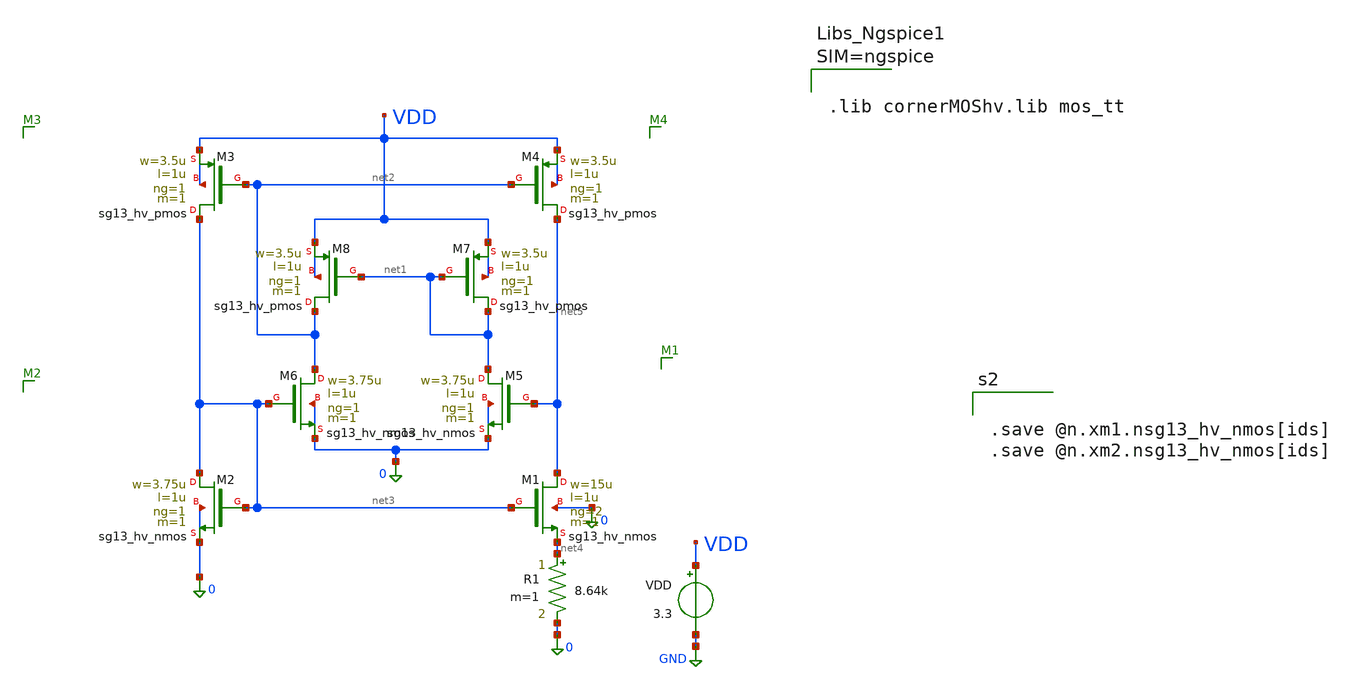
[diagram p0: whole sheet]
** sch_path: v2_bmr_bias/BMR12u5.sch
**.subckt BMR12u5
VDD VDD GND 3.3
R1 net4 0 8.64k m=1
XM1 net5 net3 net4 0 sg13_hv_nmos w=15u l=1u ng=2 m=1 mm_ok=1
XM2 net3 net3 0 0 sg13_hv_nmos w=3.75u l=1u ng=1 m=1 mm_ok=1
XM3 net3 net2 VDD VDD sg13_hv_pmos w=3.5u l=1u ng=1 m=1 mm_ok=1
XM4 net5 net2 VDD VDD sg13_hv_pmos w=3.5u l=1u ng=1 m=1 mm_ok=1
XM5 net1 net5 0 0 sg13_hv_nmos w=3.75u l=1u ng=1 m=1 mm_ok=1
XM6 net2 net3 0 0 sg13_hv_nmos w=3.75u l=1u ng=1 m=1 mm_ok=1
XM7 net1 net1 VDD VDD sg13_hv_pmos w=3.5u l=1u ng=1 m=1 mm_ok=1
XM8 net2 net1 VDD VDD sg13_hv_pmos w=3.5u l=1u ng=1 m=1 mm_ok=1
**** begin user architecture code



.lib cornerMOShv.lib mos_tt






.control
op
write BMR12u5.save
dc vdd 0 4 10m
let id1=@n.xm1.nsg13_hv_nmos[ids]
let id2=@n.xm2.nsg13_hv_nmos[ids]
plot id1 id2
.endc




.save @n.xm1.nsg13_hv_nmos[ids]
.save @n.xm2.nsg13_hv_nmos[ids]


**** end user architecture code
**.ends
.GLOBAL GND
.end
